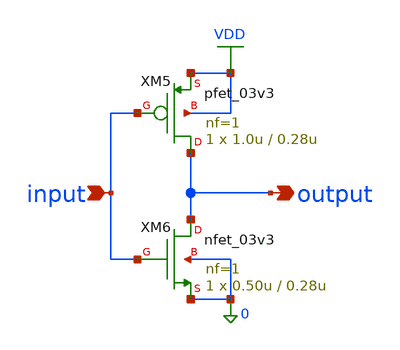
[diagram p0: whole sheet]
** sch_path: xschem/sar_adc/blocks/async_sar/async_inverter.sch
**.subckt async_inverter input output
*.ipin input
*.opin output
XM5 output input VDD VDD pfet_03v3 L=0.28u W=1.0u nf=1 ad='int((nf+1)/2) * W/nf * 0.18u' as='int((nf+2)/2) * W/nf * 0.18u'
+ pd='2*int((nf+1)/2) * (W/nf + 0.18u)' ps='2*int((nf+2)/2) * (W/nf + 0.18u)' nrd='0.18u / W' nrs='0.18u / W'
+ sa=0 sb=0 sd=0 m=1
XM6 output input 0 0 nfet_03v3 L=0.28u W=0.50u nf=1 ad='int((nf+1)/2) * W/nf * 0.18u' as='int((nf+2)/2) * W/nf * 0.18u'
+ pd='2*int((nf+1)/2) * (W/nf + 0.18u)' ps='2*int((nf+2)/2) * (W/nf + 0.18u)' nrd='0.18u / W' nrs='0.18u / W'
+ sa=0 sb=0 sd=0 m=1
**.ends
.GLOBAL VDD
.end
